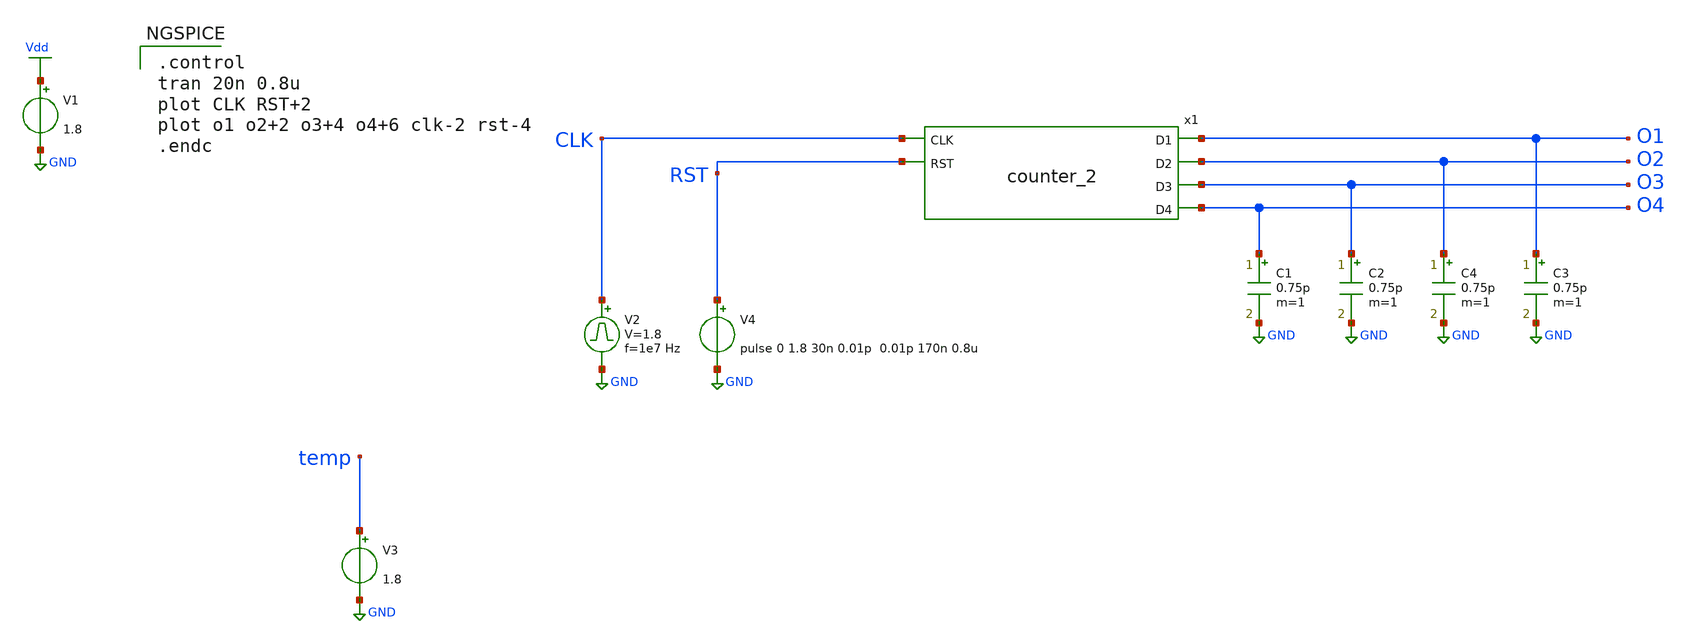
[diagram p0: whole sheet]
** sch_path: Circuiti/binary_counter_test.sch
**.subckt binary_counter_test
V1 Vdd GND 1.8
V2 CLK GND pulse 0 1.8 '0.495/ 1e7 ' '0.01/1e7 ' '0.01/1e7 ' '0.49/1e7 ' '1/1e7 '
C2 O3 GND 0.75p m=1
C1 O4 GND 0.75p m=1
C3 O1 GND 0.75p m=1
C4 O2 GND 0.75p m=1
V3 temp GND 1.8
V4 RST GND pulse 0 1.8 30n 0.01p 0.01p 170n 0.8u
x1 O1 O2 O3 O4 CLK RST counter_2
**** begin user architecture code


.lib /home/matteo/xschem_downloads/skywater-pdk/libraries/sky130_fd_pr_ngspice/latest/models/sky130.lib.spice tt

*.include /home/matteo/xschem_downloads/skywater-pdk/libraries/sky130_fd_pr_ngspice/latest/cells/nfet_01v8/sky130_fd_pr__nfet_01v8__tt.corner.spice

.param mc_mm_switch=0
.param mc_pr_switch=1



.control
tran 20n 0.8u
plot CLK RST+2
plot o1 o2+2 o3+4 o4+6 clk-2 rst-4
.endc


**** end user architecture code
**.ends

* expanding   symbol:  /home/matteo/Documenti/tesi/Circuiti/latches_sch_sym/counter_2.sym # of
*+ pins=6
** sym_path: Circuiti/latches_sch_sym/counter_2.sym
** sch_path: Circuiti/latches_sch_sym/counter_2.sch
.subckt counter_2 D1 D2 D3 D4 CLK RST
*.ipin RST
*.opin D1
*.opin D2
*.opin D3
*.opin D4
*.ipin CLK
C1 net1 GND 0.75p m=1
x13 net47 net11 RST or_2
x1 net5 net4 net3 nor_2
x2 net4 net3 net6 nor_2
x5 net13 net5 net11 and_2
x7 net11 net6 net12 and_2
x8 net11 net10 not
x14 net8 net7 D1 nor_2
x16 net7 D1 net9 nor_2
x17 net4 net8 net10 and_2
x19 net10 net9 net3 and_2
x21 D1 net13 Vdd and_2
x22 net2 net12 net7 and_2
x24 net47 net48 edg_det
x25 net49 net22 RST or_2
x26 net16 net15 net14 nor_2
x27 net15 net14 net17 nor_2
x28 net24 net16 net22 and_2
x29 net22 net17 net23 and_2
x30 net22 net21 not
x31 net19 net18 D2 nor_2
x32 net18 D2 net20 nor_2
x33 net15 net19 net21 and_2
x34 net21 net20 net14 and_2
x35 D2 net24 Vdd and_2
x36 net2 net23 net18 and_2
x37 net49 net50 edg_det
x38 net51 net33 RST or_2
x39 net27 net26 net25 nor_2
x40 net26 net25 net28 nor_2
x41 net35 net27 net33 and_2
x42 net33 net28 net34 and_2
x43 net33 net32 not
x44 net30 net29 D3 nor_2
x45 net29 D3 net31 nor_2
x46 net26 net30 net32 and_2
x47 net32 net31 net25 and_2
x48 D3 net35 Vdd and_2
x49 net2 net34 net29 and_2
x50 net51 net52 edg_det
x51 net53 net43 RST or_2
x52 net38 net37 net36 nor_2
x53 net37 net36 net39 nor_2
x54 net45 net38 net43 and_2
x55 net43 net39 net44 and_2
x56 net43 net42 not
x57 net40 net1 D4 nor_2
x58 net1 D4 net41 nor_2
x59 net37 net40 net42 and_2
x60 net42 net41 net36 and_2
x61 D4 net45 Vdd and_2
x62 net2 net44 net1 and_2
x63 net53 net54 edg_det
x10 RST net46 not
x4 CLK net48 net46 and_2
x3 net46 net50 net7 and_2
x6 net46 net52 net18 and_2
x9 net46 net54 net29 and_2
.ends


* expanding   symbol:  /home/matteo/Documenti/tesi/Circuiti/logic_gates_sch_sym/or_2.sym # of pins=3
** sym_path: Circuiti/logic_gates_sch_sym/or_2.sym
** sch_path: Circuiti/logic_gates_sch_sym/or_2.sch
.subckt or_2 A Y B
*.ipin A
*.ipin B
*.opin Y
x1 A net1 B nor_2
x2 net1 Y not
.ends


* expanding   symbol:  /home/matteo/Documenti/tesi/Circuiti/logic_gates_sch_sym/nor_2.sym # of
*+ pins=3
** sym_path: Circuiti/logic_gates_sch_sym/nor_2.sym
** sch_path: Circuiti/logic_gates_sch_sym/nor_2.sch
.subckt nor_2 A Y B
*.opin Y
*.ipin A
*.ipin B
XM1 Y B GND GND sky130_fd_pr__nfet_01v8 L=0.45 W=1 nf=1 ad='int((nf+1)/2) * W/nf * 0.29' as='int((nf+2)/2) * W/nf * 0.29'
+ pd='2*int((nf+1)/2) * (W/nf + 0.29)' ps='2*int((nf+2)/2) * (W/nf + 0.29)' nrd='0.29 / W' nrs='0.29 / W'
+ sa=0 sb=0 sd=0 mult=1 m=1
XM3 Y B net1 VDD sky130_fd_pr__pfet_01v8 L=0.15 W=4.8 nf=1 ad='int((nf+1)/2) * W/nf * 0.29' as='int((nf+2)/2) * W/nf * 0.29'
+ pd='2*int((nf+1)/2) * (W/nf + 0.29)' ps='2*int((nf+2)/2) * (W/nf + 0.29)' nrd='0.29 / W' nrs='0.29 / W'
+ sa=0 sb=0 sd=0 mult=1 m=1
XM4 net1 A Vdd VDD sky130_fd_pr__pfet_01v8 L=0.15 W=4.8 nf=1 ad='int((nf+1)/2) * W/nf * 0.29' as='int((nf+2)/2) * W/nf * 0.29'
+ pd='2*int((nf+1)/2) * (W/nf + 0.29)' ps='2*int((nf+2)/2) * (W/nf + 0.29)' nrd='0.29 / W' nrs='0.29 / W'
+ sa=0 sb=0 sd=0 mult=1 m=1
XM2 Y A GND GND sky130_fd_pr__nfet_01v8 L=0.45 W=1 nf=1 ad='int((nf+1)/2) * W/nf * 0.29' as='int((nf+2)/2) * W/nf * 0.29'
+ pd='2*int((nf+1)/2) * (W/nf + 0.29)' ps='2*int((nf+2)/2) * (W/nf + 0.29)' nrd='0.29 / W' nrs='0.29 / W'
+ sa=0 sb=0 sd=0 mult=1 m=1
.ends


* expanding   symbol:  /home/matteo/Documenti/tesi/Circuiti/logic_gates_sch_sym/and_2.sym # of
*+ pins=3
** sym_path: Circuiti/logic_gates_sch_sym/and_2.sym
** sch_path: Circuiti/logic_gates_sch_sym/and_2.sch
.subckt and_2 A Y B
*.ipin B
*.ipin A
*.opin Y
x1 A net1 B nand_2
x2 net1 Y not
.ends


* expanding   symbol:  /home/matteo/Documenti/tesi/Circuiti/logic_gates_sch_sym/not.sym # of pins=2
** sym_path: Circuiti/logic_gates_sch_sym/not.sym
** sch_path: Circuiti/logic_gates_sch_sym/not.sch
.subckt not A Y
*.ipin A
*.opin Y
XM1 Y A GND GND sky130_fd_pr__nfet_01v8 L=0.45 W=1 nf=1 ad='int((nf+1)/2) * W/nf * 0.29' as='int((nf+2)/2) * W/nf * 0.29'
+ pd='2*int((nf+1)/2) * (W/nf + 0.29)' ps='2*int((nf+2)/2) * (W/nf + 0.29)' nrd='0.29 / W' nrs='0.29 / W'
+ sa=0 sb=0 sd=0 mult=1 m=1
XM2 Y A Vdd VDD sky130_fd_pr__pfet_01v8 L=0.45 W=4.8 nf=1 ad='int((nf+1)/2) * W/nf * 0.29' as='int((nf+2)/2) * W/nf * 0.29'
+ pd='2*int((nf+1)/2) * (W/nf + 0.29)' ps='2*int((nf+2)/2) * (W/nf + 0.29)' nrd='0.29 / W' nrs='0.29 / W'
+ sa=0 sb=0 sd=0 mult=1 m=1
.ends


* expanding   symbol:  /home/matteo/Documenti/tesi/Circuiti/latches_sch_sym/edg_det.sym # of pins=2
** sym_path: Circuiti/latches_sch_sym/edg_det.sym
** sch_path: Circuiti/latches_sch_sym/edg_det.sch
.subckt edg_det OUT CLK
*.ipin CLK
*.opin OUT
x3 CLK net1 not
C3 net1 GND 1.5p m=1
x1 CLK OUT net1 and_2
.ends


* expanding   symbol:  /home/matteo/Documenti/tesi/Circuiti/logic_gates_sch_sym/nand_2.sym # of
*+ pins=3
** sym_path: Circuiti/logic_gates_sch_sym/nand_2.sym
** sch_path: Circuiti/logic_gates_sch_sym/nand_2.sch
.subckt nand_2 A Y B
*.ipin A
*.ipin B
*.opin Y
XM1 Y A net1 GND sky130_fd_pr__nfet_01v8 L=0.15 W=1 nf=1 ad='int((nf+1)/2) * W/nf * 0.29' as='int((nf+2)/2) * W/nf * 0.29'
+ pd='2*int((nf+1)/2) * (W/nf + 0.29)' ps='2*int((nf+2)/2) * (W/nf + 0.29)' nrd='0.29 / W' nrs='0.29 / W'
+ sa=0 sb=0 sd=0 mult=1 m=1
XM3 Y B Vdd VDD sky130_fd_pr__pfet_01v8 L=0.45 W=4.8 nf=1 ad='int((nf+1)/2) * W/nf * 0.29' as='int((nf+2)/2) * W/nf * 0.29'
+ pd='2*int((nf+1)/2) * (W/nf + 0.29)' ps='2*int((nf+2)/2) * (W/nf + 0.29)' nrd='0.29 / W' nrs='0.29 / W'
+ sa=0 sb=0 sd=0 mult=1 m=1
XM4 Y A Vdd VDD sky130_fd_pr__pfet_01v8 L=0.45 W=4.8 nf=1 ad='int((nf+1)/2) * W/nf * 0.29' as='int((nf+2)/2) * W/nf * 0.29'
+ pd='2*int((nf+1)/2) * (W/nf + 0.29)' ps='2*int((nf+2)/2) * (W/nf + 0.29)' nrd='0.29 / W' nrs='0.29 / W'
+ sa=0 sb=0 sd=0 mult=1 m=1
XM2 net1 B GND GND sky130_fd_pr__nfet_01v8 L=0.15 W=1 nf=1 ad='int((nf+1)/2) * W/nf * 0.29' as='int((nf+2)/2) * W/nf * 0.29'
+ pd='2*int((nf+1)/2) * (W/nf + 0.29)' ps='2*int((nf+2)/2) * (W/nf + 0.29)' nrd='0.29 / W' nrs='0.29 / W'
+ sa=0 sb=0 sd=0 mult=1 m=1
.ends

.GLOBAL GND
.GLOBAL Vdd
.end
